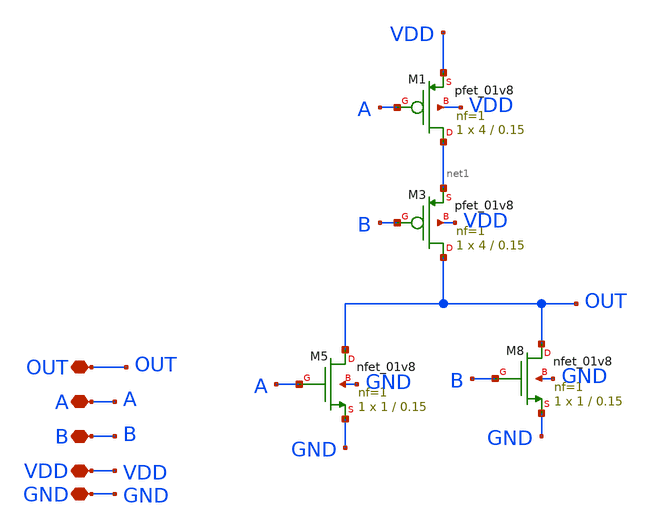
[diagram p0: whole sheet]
** sch_path: xschem/nand.sch
**.subckt nand VDD GND B A OUT
*.iopin VDD
*.iopin GND
*.iopin B
*.iopin A
*.iopin OUT
XM1 net1 A VDD VDD sky130_fd_pr__pfet_01v8 L=0.15 W=4 nf=1 ad='int((nf+1)/2) * W/nf * 0.29' as='int((nf+2)/2) * W/nf * 0.29'
+ pd='2*int((nf+1)/2) * (W/nf + 0.29)' ps='2*int((nf+2)/2) * (W/nf + 0.29)' nrd='0.29 / W' nrs='0.29 / W'
+ sa=0 sb=0 sd=0 mult=1 m=1
XM3 OUT B net1 VDD sky130_fd_pr__pfet_01v8 L=0.15 W=4 nf=1 ad='int((nf+1)/2) * W/nf * 0.29' as='int((nf+2)/2) * W/nf * 0.29'
+ pd='2*int((nf+1)/2) * (W/nf + 0.29)' ps='2*int((nf+2)/2) * (W/nf + 0.29)' nrd='0.29 / W' nrs='0.29 / W'
+ sa=0 sb=0 sd=0 mult=1 m=1
XM5 OUT A GND GND sky130_fd_pr__nfet_01v8 L=0.15 W=1 nf=1 ad='int((nf+1)/2) * W/nf * 0.29' as='int((nf+2)/2) * W/nf * 0.29'
+ pd='2*int((nf+1)/2) * (W/nf + 0.29)' ps='2*int((nf+2)/2) * (W/nf + 0.29)' nrd='0.29 / W' nrs='0.29 / W'
+ sa=0 sb=0 sd=0 mult=1 m=1
XM8 OUT B GND GND sky130_fd_pr__nfet_01v8 L=0.15 W=1 nf=1 ad='int((nf+1)/2) * W/nf * 0.29' as='int((nf+2)/2) * W/nf * 0.29'
+ pd='2*int((nf+1)/2) * (W/nf + 0.29)' ps='2*int((nf+2)/2) * (W/nf + 0.29)' nrd='0.29 / W' nrs='0.29 / W'
+ sa=0 sb=0 sd=0 mult=1 m=1
**.ends
.end
